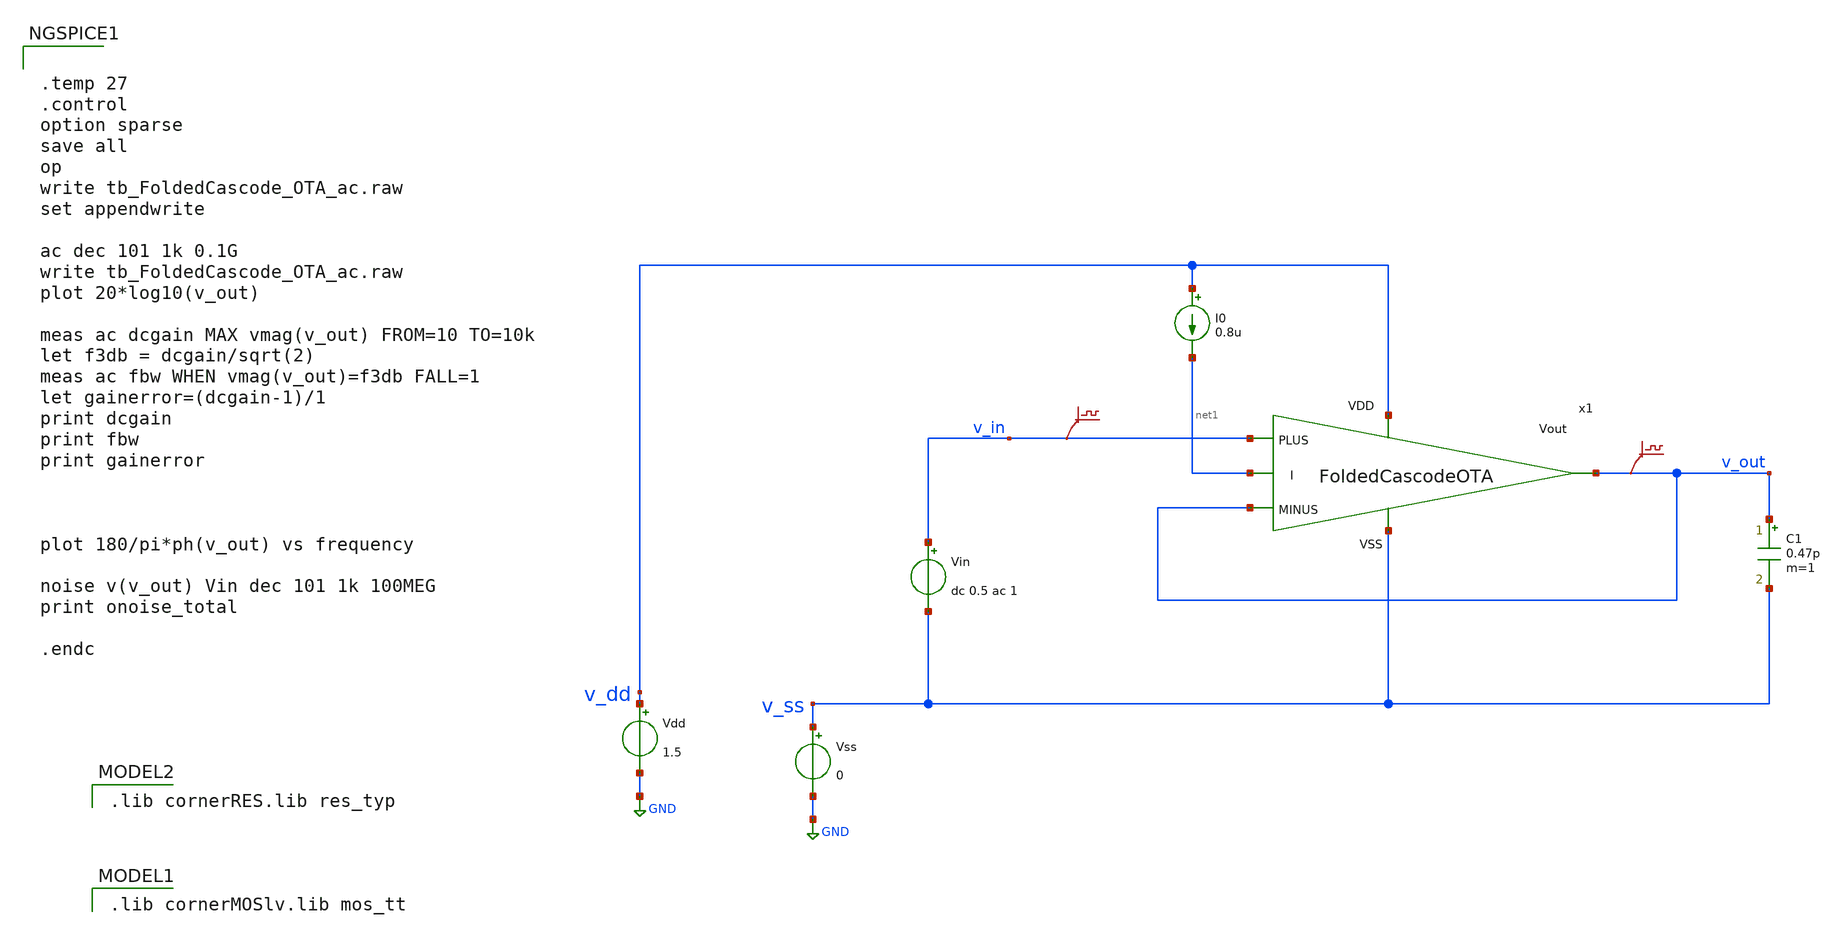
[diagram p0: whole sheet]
** sch_path: DSM/Schematics/RealCircuits/Folded Cascode/tb_FolCas_ac.sch
* (c) 2024 Hrishikesh, @HSB
**.subckt tb_FolCas_ac
Vss v_ss GND 0
Vdd v_dd GND 1.5
Vin v_in v_ss dc 0.5 ac 1
.save v(v_in)
I0 v_dd net1 0.8u
C1 v_out v_ss 0.47p m=1
.save v(v_out)
x1 v_dd net1 v_in v_out v_out v_ss FoldedCascodeOTA
**** begin user architecture code
 .lib cornerMOSlv.lib mos_tt

 .lib cornerRES.lib res_typ



.temp 27
.control
option sparse
save all
op
write tb_FoldedCascode_OTA_ac.raw
set appendwrite

ac dec 101 1k 0.1G
write tb_FoldedCascode_OTA_ac.raw
plot 20*log10(v_out)

meas ac dcgain MAX vmag(v_out) FROM=10 TO=10k
let f3db = dcgain/sqrt(2)
meas ac fbw WHEN vmag(v_out)=f3db FALL=1
let gainerror=(dcgain-1)/1
print dcgain
print fbw
print gainerror



plot 180/pi*ph(v_out) vs frequency

noise v(v_out) Vin dec 101 1k 100MEG
print onoise_total

.endc


**** end user architecture code
**.ends

* expanding   symbol:  /foss/designs/CEMS_DSM/DSM/Schematics/Designs_Hrishi/RealCircuits/Folded
*+ Cascode/FoldedCascodeOTA.sym # of pins=6
** sym_path: DSM/Schematics/IC_Designs_Hrishi/RealCircuits/Folded Cascode/FoldedCascodeOTA.sym
** sch_path: DSM/Schematics/IC_Designs_Hrishi/RealCircuits/Folded Cascode/FoldedCascodeOTA.sch
.subckt FoldedCascodeOTA VDD I PLUS MINUS Vout VSS
*.ipin PLUS
*.ipin MINUS
*.opin Vout
*.ipin VDD
*.ipin VSS
*.ipin I
XM1 net2 net4 VDD VDD sg13_lv_pmos w=0.272u l=0.5u ng=1 m=1 mm_ok=1
XM2 net1 PLUS net2 VDD sg13_lv_pmos w=0.136u l=0.5u ng=1 m=1 mm_ok=1
XM3 net6 MINUS net2 VDD sg13_lv_pmos w=0.136u l=0.5u ng=1 m=1 mm_ok=1
XM14 net6 net9 VSS VSS sg13_lv_nmos w=0.30u l=2u ng=1 m=1 mm_ok=1
XM13 Vout I net6 VSS sg13_lv_nmos w=0.15u l=2u ng=1 m=1 mm_ok=1
XM11 net7 I net1 VSS sg13_lv_nmos w=0.15u l=2u ng=1 m=1 mm_ok=1
XM12 net1 net9 VSS VSS sg13_lv_nmos w=0.30u l=2u ng=1 m=1 mm_ok=1
XM5 Vout net3 net5 VDD sg13_lv_pmos w=0.136u l=0.5u ng=1 m=1 mm_ok=1
XM4 net5 net4 VDD VDD sg13_lv_pmos w=0.136u l=0.5u ng=1 m=1 mm_ok=1
XM6 net4 net4 VDD VDD sg13_lv_pmos w=0.136u l=0.5u ng=1 m=1 mm_ok=1
XM8 net3 net3 net4 VDD sg13_lv_pmos w=0.136u l=0.5u ng=1 m=1 mm_ok=1
XM9 net8 net4 VDD VDD sg13_lv_pmos w=0.136u l=0.5u ng=1 m=1 mm_ok=1
XM10 net7 net3 net8 VDD sg13_lv_pmos w=0.136u l=0.5u ng=1 m=1 mm_ok=1
XM16 I I net9 VSS sg13_lv_nmos w=0.15u l=2u ng=1 m=1 mm_ok=1
XM15 net9 net9 VSS VSS sg13_lv_nmos w=0.15u l=2u ng=1 m=1 mm_ok=1
XM7 net3 net9 VSS VSS sg13_lv_nmos w=0.15u l=2u ng=1 m=1 mm_ok=1
XM18 VDD I net10 VSS sg13_lv_nmos w=0.15u l=2u ng=1 m=1 mm_ok=1
XM17 net10 net9 VSS VSS sg13_lv_nmos w=0.15u l=2u ng=1 m=1 mm_ok=1
.ends

.GLOBAL GND
.end
